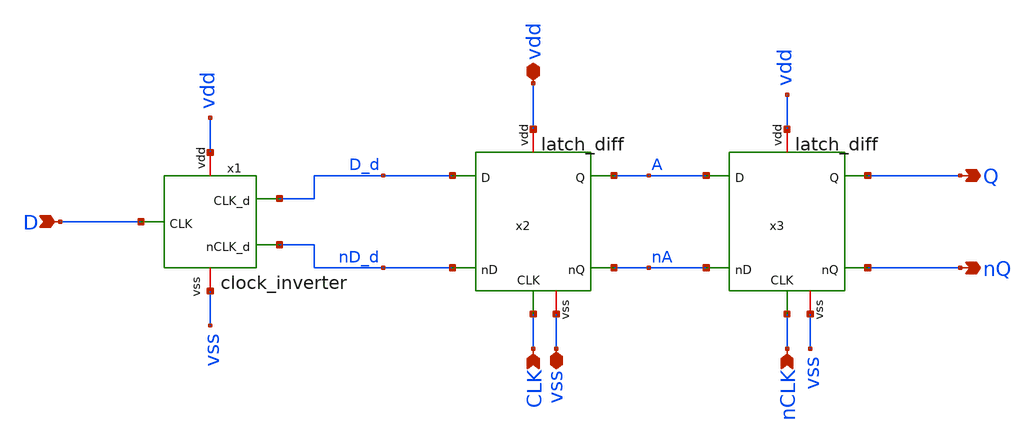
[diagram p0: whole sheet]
** sch_path: xschem/afernandez_residue_amplifier/DFlipFlop.sch
**.subckt DFlipFlop vdd vss Q nQ D CLK nCLK
*.iopin vdd
*.iopin vss
*.opin Q
*.opin nQ
*.ipin D
*.ipin CLK
*.ipin nCLK
x1 vdd D_d D nD_d vss clock_inverter
x2 vdd nA A D_d nD_d CLK vss latch_diff
x3 vdd nQ Q A nA nCLK vss latch_diff
**.ends
.end
